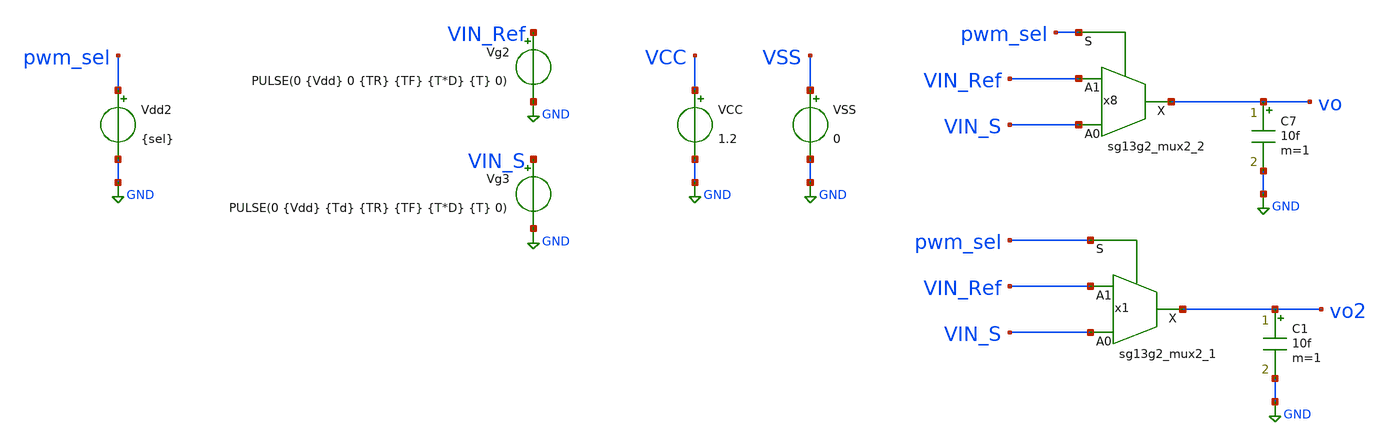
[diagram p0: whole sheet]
** sch_path: ChipUSM_AnalogTrack24/Mux/TB_Mux.sch
* IHP-GmbH/IHP-Open-PDK/ihp-sg13g2/libs.tech/xschem/sg13g2_stdcells/sg13g2_mux2_1.sch:
* Copyright 2023 IHP PDK Authors
* Licensed under the Apache License, Version 2.0 (the "License");
**.subckt TB_Mux
x8 vo VIN_S VIN_Ref pwm_sel VCC VSS sg13g2_mux2_2
Vdd2 pwm_sel GND {sel}
Vg2 VIN_Ref GND PULSE(0 {Vdd} 0 {TR} {TF} {T*D} {T} 0)
Vg3 VIN_S GND PULSE(0 {Vdd} {Td} {TR} {TF} {T*D} {T} 0)
C7 vo GND 10f m=1
x1 vo2 VIN_S VIN_Ref pwm_sel VDD VSS sg13g2_mux2_1
C1 vo2 GND 10f m=1
VCC VCC GND 1.2
VSS VSS GND 0
**** begin user architecture code


*.lib cornerMOShv.lib mos_tt
*.lib cornerMOSlv.lib mos_tt
*.lib cornerMOShv.lib mos_ff
*.lib cornerMOSlv.lib mos_ff
.lib cornerMOShv.lib mos_ss
.lib cornerMOSlv.lib mos_ss
*.lib cornerMOShv.lib mos_sf
*.lib cornerMOSlv.lib mos_sf
*.lib cornerMOShv.lib mos_fs
*.lib cornerMOSlv.lib mos_fs

.include /opt/pdks/ihp-sg13g2/libs.ref/sg13g2_stdcell/spice/sg13g2_stdcell.spice
.lib $::SG13G2_MODELS/cornerRES.lib res_typ
.lib $::SG13G2_MODELS/cornerCAP.lib cap_typ




.param Vdd = 1.2
.param VH = 3.3
.param Del = 0
*.param sel = 1.2
.param sel = 0

*.param D = 0.6364
.param D = 0.615
.param TR = 1p
.param TF = 1p
.param Td = D*T
.param TdR = 2n
.param TdF = 2n

*fs = 10MHz
*.param T = 0.1u
*fs = 8.4MHz
.param T = 0.11905u

*.param temp = 27
*.param temp = -40
.param temp = 125





.save all  @n.x1.xm1.nsg13_hv_pmos[ids]  @n.x1.xm2.nsg13_hv_nmos[ids]
.param SimTime = 5u

.option method=gear

.control
reset
set color0 = white
tran 100p 1u
plot v(VIN_Ref) v(VIN_S)+1.5 v(vo)+3
plot v(VIN_Ref) v(VIN_S)+1.5 v(vo2)+3
.endc



.end


**** end user architecture code
**.ends

* expanding   symbol:  sg13g2_stdcells/sg13g2_mux2_2.sym # of pins=4
** sym_path: sg13g2_stdcells/sg13g2_mux2_2.sym
** sch_path: sg13g2_stdcells/sg13g2_mux2_2.sch
.subckt sg13g2_mux2_2 X A0 A1 S VDD VSS
*.ipin S
*.ipin A0
*.ipin A1
*.opin X
*.iopin VDD
*.iopin VSS
XM1 Sb S VSS VSS sg13_lv_nmos w=550.00n l=130.00n ng=1 m=1 mm_ok=1
XM2 net1 A0 net5 VSS sg13_lv_nmos w=740.00n l=130.00n ng=1 m=1 mm_ok=1
XM3 net5 Sb VSS VSS sg13_lv_nmos w=740.00n l=130.00n ng=1 m=1 mm_ok=1
XM4 net1 A1 net4 VSS sg13_lv_nmos w=740.00n l=130.00n ng=1 m=1 mm_ok=1
XM5 net4 S VSS VSS sg13_lv_nmos w=740.00n l=130.00n ng=1 m=1 mm_ok=1
XM6 X net1 VSS VSS sg13_lv_nmos w=1.48u l=130.00n ng=2 m=1 mm_ok=1
XM7 Sb S VDD VDD sg13_lv_pmos w=840.00n l=130.00n ng=1 m=1 mm_ok=1
XM8 net2 S VDD VDD sg13_lv_pmos w=1.000u l=130.00n ng=1 m=1 mm_ok=1
XM9 net1 A0 net2 VDD sg13_lv_pmos w=1.000u l=130.00n ng=1 m=1 mm_ok=1
XM10 net3 Sb VDD VDD sg13_lv_pmos w=1.000u l=130.00n ng=1 m=1 mm_ok=1
XM11 net1 A1 net3 VDD sg13_lv_pmos w=1.000u l=130.00n ng=1 m=1 mm_ok=1
XM12 X net1 VDD VDD sg13_lv_pmos w=2.24u l=130.00n ng=2 m=1 mm_ok=1
.ends


* expanding   symbol:  sg13g2_stdcells/sg13g2_mux2_1.sym # of pins=4
** sym_path: sg13g2_stdcells/sg13g2_mux2_1.sym
** sch_path: sg13g2_stdcells/sg13g2_mux2_1.sch
.subckt sg13g2_mux2_1 X A0 A1 S VDD VSS
*.ipin S
*.ipin A0
*.ipin A1
*.opin X
*.iopin VDD
*.iopin VSS
XM1 Sb S VSS VSS sg13_lv_nmos w=550.00n l=130.00n ng=1 m=1 mm_ok=1
XM2 net1 A0 net5 VSS sg13_lv_nmos w=740.00n l=130.00n ng=1 m=1 mm_ok=1
XM3 net5 Sb VSS VSS sg13_lv_nmos w=740.00n l=130.00n ng=1 m=1 mm_ok=1
XM4 net1 A1 net4 VSS sg13_lv_nmos w=740.00n l=130.00n ng=1 m=1 mm_ok=1
XM5 net4 S VSS VSS sg13_lv_nmos w=740.00n l=130.00n ng=1 m=1 mm_ok=1
XM6 X net1 VSS VSS sg13_lv_nmos w=740.00n l=130.00n ng=1 m=1 mm_ok=1
XM7 Sb S VDD VDD sg13_lv_pmos w=840.00n l=130.00n ng=1 m=1 mm_ok=1
XM8 net2 S VDD VDD sg13_lv_pmos w=1.000u l=130.00n ng=1 m=1 mm_ok=1
XM9 net1 A0 net2 VDD sg13_lv_pmos w=1.000u l=130.00n ng=1 m=1 mm_ok=1
XM10 net3 Sb VDD VDD sg13_lv_pmos w=1.000u l=130.00n ng=1 m=1 mm_ok=1
XM11 net1 A1 net3 VDD sg13_lv_pmos w=1.000u l=130.00n ng=1 m=1 mm_ok=1
XM12 X net1 VDD VDD sg13_lv_pmos w=1.12u l=130.00n ng=1 m=1 mm_ok=1
.ends

.GLOBAL GND
.end
